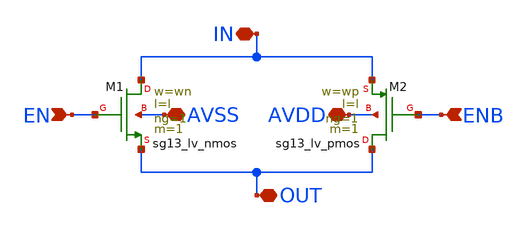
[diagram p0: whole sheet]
** sch_path: xschem/tgate/tgate.sch
**.subckt tgate AVDD AVSS IN OUT EN ENB
*.iopin AVDD
*.iopin AVSS
*.iopin IN
*.iopin OUT
*.ipin EN
*.ipin ENB
XM1 IN EN OUT AVSS sg13_lv_nmos w=wn l=l ng=1 m=1 mm_ok=1
XM2 OUT ENB IN AVDD sg13_lv_pmos w=wp l=l ng=1 m=1 mm_ok=1
**.ends
.end
